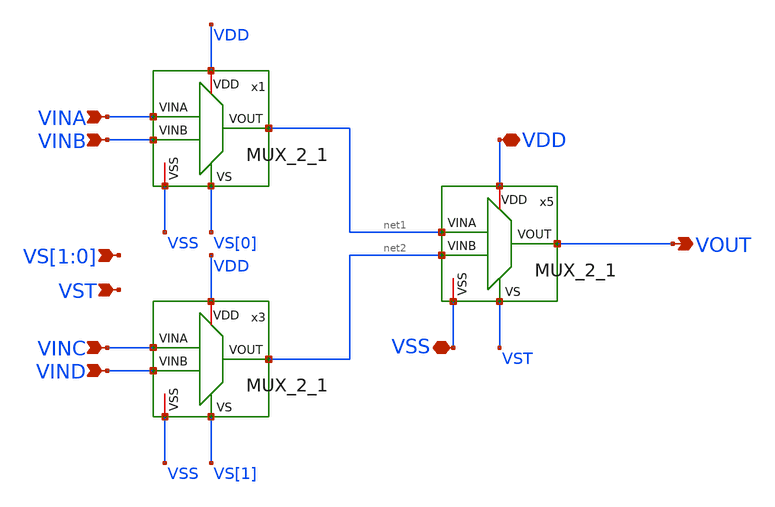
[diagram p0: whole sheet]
** sch_path: CDR4176-main/schematic/xschem/MUX_4_1/MUX_4_1.sch
**.subckt MUX_4_1 VOUT VDD VSS VINA VINB VINC VIND VS[1],VS[0] VST
*.opin VOUT
*.iopin VDD
*.iopin VSS
*.ipin VINA
*.ipin VINB
*.ipin VINC
*.ipin VIND
*.ipin VS[1],VS[0]
*.ipin VST
x3 VDD VINC net2 VS[1] VIND VSS MUX_2_1
x5 VDD net1 VOUT VST net2 VSS MUX_2_1
x1 VDD VINA net1 VS[0] VINB VSS MUX_2_1
**.ends
.end
